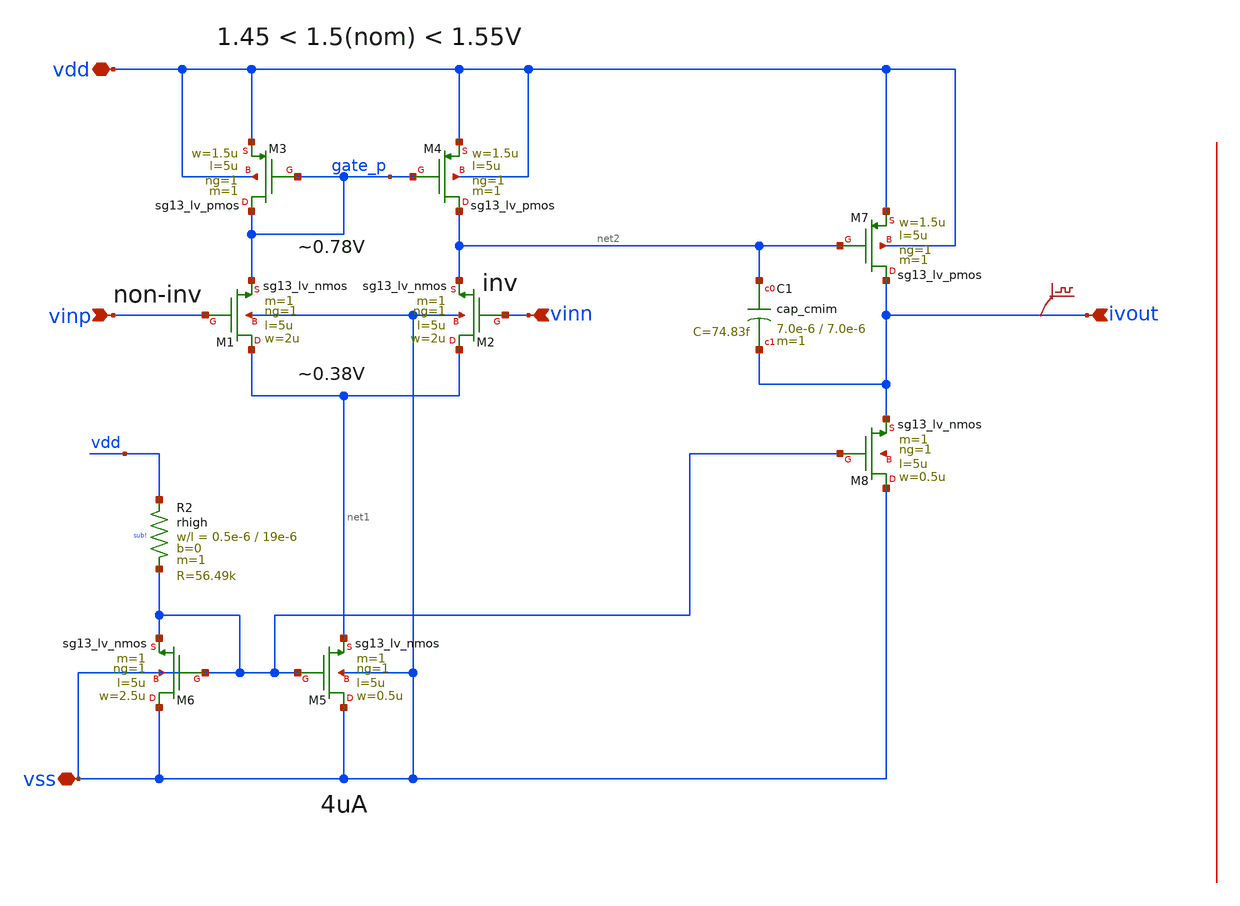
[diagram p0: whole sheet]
** sch_path: 3_Real_Cir/10_Real_Cir/test_Real_Cir/Improved/improved_5t_ota_A.sch
* Copyright 2023 IHP PDK Authors
* Licensed under the Apache License, Version 2.0 (the "License");
* you may not use this file except in compliance with the License.
* You may obtain a copy of the License at
* https://www.apache.org/licenses/LICENSE-2.0
* Unless required by applicable law or agreed to in writing, software
* distributed under the License is distributed on an "AS IS" BASIS,
* WITHOUT WARRANTIES OR CONDITIONS OF ANY KIND, either express or implied.
* See the License for the specific language governing permissions and
* limitations under the License.
* Copyright 2024 IHP PDK Authors
**.subckt improved_5t_ota_A vdd vss vinp vinn ivout
*.iopin vdd
*.iopin vss
*.ipin vinp
*.ipin vinn
*.ipin ivout
.save v(ivout)
XM5 vss vss net1 vss sg13_lv_nmos w=0.5u l=5u ng=1 m=1 mm_ok=1
XM4 net2 gate_p vdd vdd sg13_lv_pmos w=1.5u l=5u ng=1 m=1 mm_ok=1
XM1 net1 vinp gate_p vss sg13_lv_nmos w=2u l=5u ng=1 m=1 mm_ok=1
XM2 net1 vinn net2 vss sg13_lv_nmos w=2u l=5u ng=1 m=1 mm_ok=1
XM3 gate_p gate_p vdd vdd sg13_lv_pmos w=1.5u l=5u ng=1 m=1 mm_ok=1
XM6 vss vss vss vss sg13_lv_nmos w=2.5u l=5u ng=1 m=1 mm_ok=1
XR2 vdd vss sub! rhigh w=0.5e-6 l=19e-6 m=1 b=0 mm_ok=1
XM7 ivout net2 vdd vdd sg13_lv_pmos w=1.5u l=5u ng=1 m=1 mm_ok=1
XM8 vss vss ivout net3 sg13_lv_nmos w=0.5u l=5u ng=1 m=1 mm_ok=1
XC1 net2 ivout cap_cmim w=7.0e-6 l=7.0e-6 m=1 mm_ok=1
**.ends
.end
